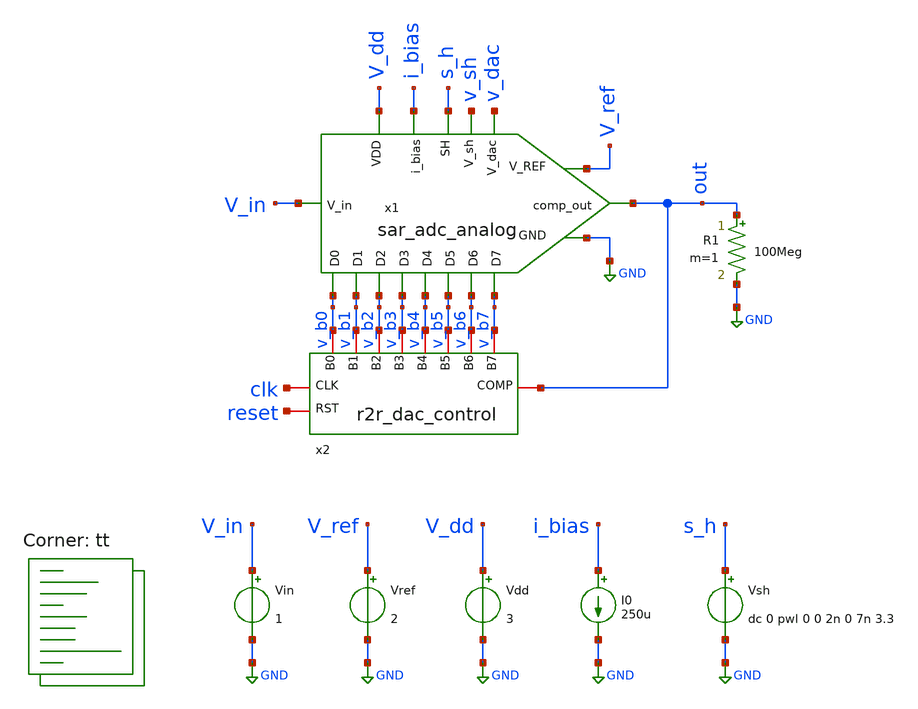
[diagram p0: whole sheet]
** sch_path: xschem/tb_sar_adc.sch
**.subckt tb_sar_adc
Vin V_in GND 1
x1 s_h V_in out i_bias v_b0 V_dd v_b1 v_b2 v_b3 GND v_b4 V_ref v_b5 v_b6 v_b7 v_sh v_dac
+ sar_adc_analog
Vref V_ref GND 2
R1 out GND 100Meg m=1
Vdd V_dd GND 3
I0 i_bias GND 250u
x2 reset clk out v_b7 v_b6 v_b5 v_b4 v_b3 v_b2 v_b1 v_b0 r2r_dac_control
Vsh s_h GND dc 0 pwl 0 0 2n 0 7n 3.3
**** begin user architecture code
.lib $::SKYWATER_MODELS/sky130.lib.spice tt


.option chgtol=4e-16

*.param TEMPGAUSS = agauss(30, 40, 1)
*.option temp = 'TEMPGAUSS'
*.param DELTA = 0.002

* .param vdda 3.3
.option TNOM=27 GMIN=1e-15 reltol=1e-3 method=gear
.param TRF = 100p
.param AVDD = 3.3
.param PERIOD_CLK = 40n
.param PW_CLK = PERIOD_CLK/2



* VCLK clk 0 dc 0 pulse (0 3.3 0 10p 10p 500n 1u)
VCLK clk 0 dc 0 pulse (0 {AVDD} 0 {TRF} {TRF} {PW_CLK} {PERIOD_CLK})
VRESET reset 0 dc {AVDD} pwl 0 {AVDD} {PW_CLK*4} {AVDD} {PW_CLK*2 + 1n} 0


.control

set num_threads=8
unset askquit

*- Override the default digital output bridge.
pre_set auto_bridge_d_out =
     + ( ".model auto_dac dac_bridge(out_low = 0.0 out_high = 1.8)"
     +   "auto_bridge%d [ %s ] [ %s ] auto_dac" )
save all
tran 1n 450n
write tb_sar_adc.raw
reset


.endc




*.include ./../cosim/r2r_dac_control.spice

.subckt r2r_dac_control reset clk comp b7 b6 b5 b4 b3 b2 b1 b0

adut [clk  reset  comp  ]  [b7  b6  b5  b4  b3  b2  b1  b0  ] null r2r_ctrl

.model r2r_ctrl d_cosim
+ simulation="/home/ttuser/tinytapeout/TT_Project/verilog/sim/r2r_dac_control.so" delay=10p
.ends r2r_dac_control


**** end user architecture code
**.ends
.GLOBAL GND
.end
